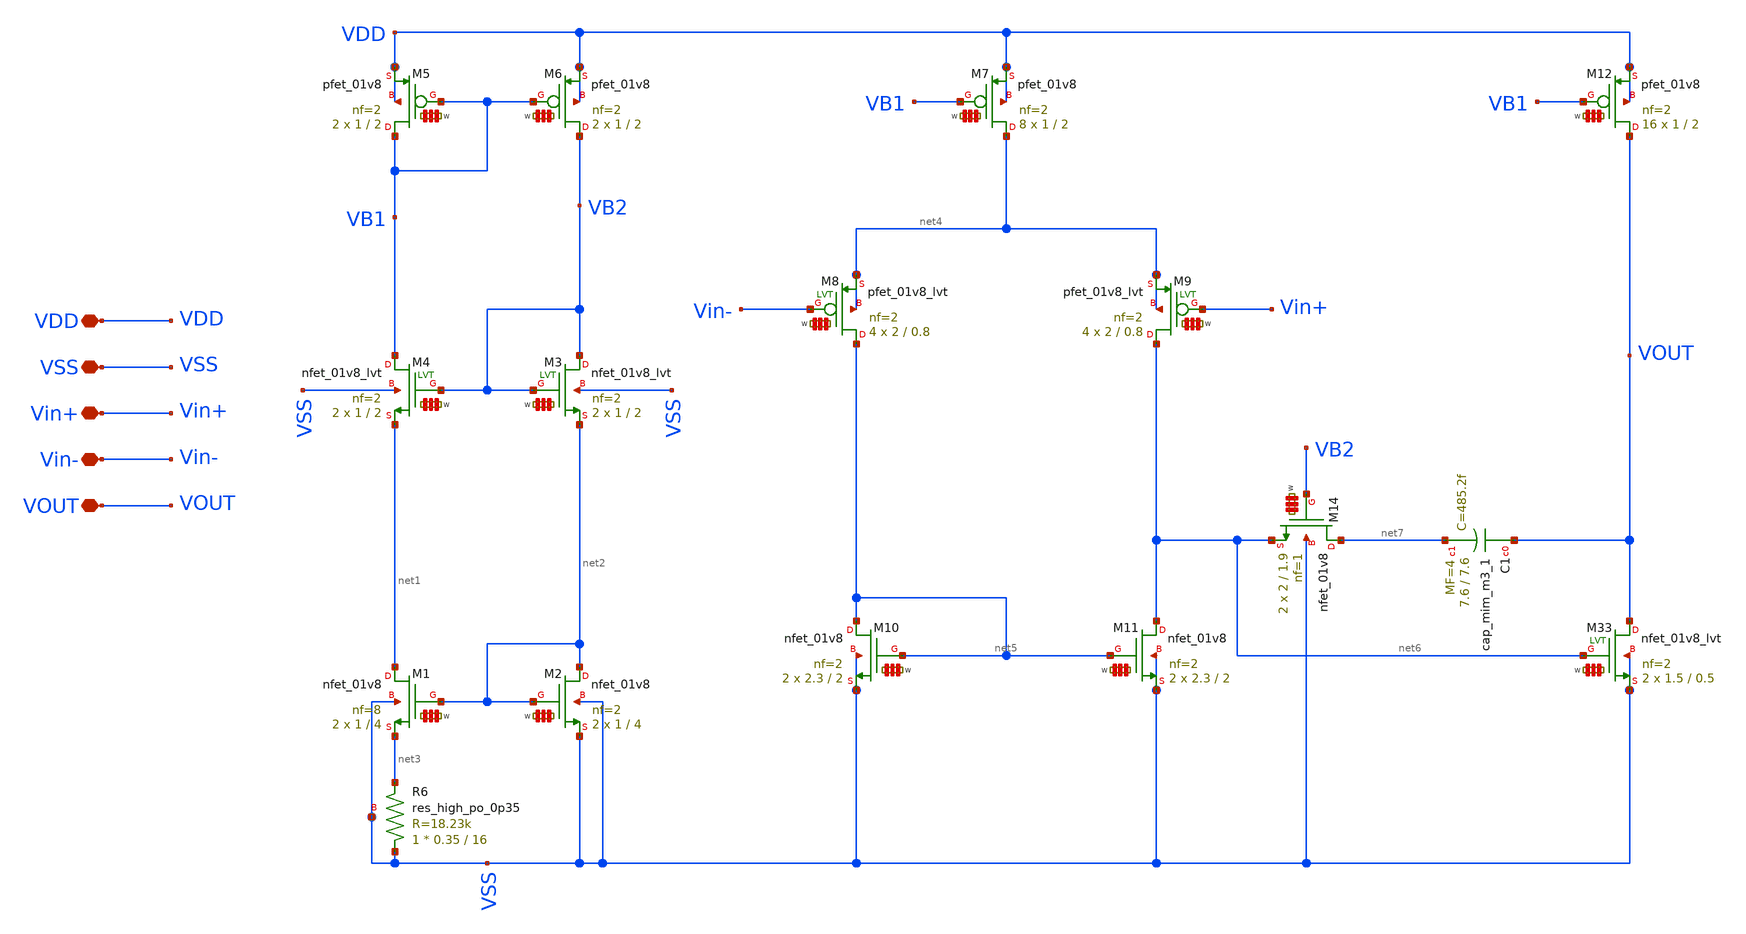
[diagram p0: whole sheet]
** sch_path: LIB/Sky130A/single ended amplifiers/VA001_sky130_1_8V.sch
**.subckt VA001_sky130_1_8V VDD VSS Vin+ Vin- VOUT
*.iopin VDD
*.iopin VSS
*.iopin Vin+
*.iopin Vin-
*.iopin VOUT
XR6 VSS net3 VSS sky130_fd_pr__res_high_po_0p35 L=16 mult=1 m=1
XM1 net1 net2 net3 VSS sky130_fd_pr__nfet_01v8 L=4 W='1 * 8 ' nf=8 ad='int((8 + 1)/2) * 1 / 8 * 0.29'
+ as='int((8 + 2)/2) * 1 / 8 * 0.29' pd='2*int((8 + 1)/2) * (1 / 8 + 0.29)' ps='2*int((8 + 2)/2) * (1 / 8 + 0.29)'
+ nrd='0.29 / 1 ' nrs='0.29 / 1 ' sa=0 sb=0 sd=0 mult=2 m=2
XM2 net2 net2 VSS VSS sky130_fd_pr__nfet_01v8 L=4 W='1 * 2 ' nf=2 ad='int((2 + 1)/2) * 1 / 2 * 0.29'
+ as='int((2 + 2)/2) * 1 / 2 * 0.29' pd='2*int((2 + 1)/2) * (1 / 2 + 0.29)' ps='2*int((2 + 2)/2) * (1 / 2 + 0.29)'
+ nrd='0.29 / 1 ' nrs='0.29 / 1 ' sa=0 sb=0 sd=0 mult=2 m=2
XM5 VB1 VB1 VDD VDD sky130_fd_pr__pfet_01v8 L=2 W='1 * 2 ' nf=2 ad= as='int((2 + 2)/2) * 1 * 0.29' pd='2*int((2 + 1)/2) * (1 + 0.29)'
+ ps='2*int((2 + 2)/2) * (1 + 0.29)' nrd='0.29 / 1 / 2 ' nrs='0.29 / 1 / 2 ' sa=0 sb=0 sd=0 mult=2 m=2
XM6 VB2 VB1 VDD VDD sky130_fd_pr__pfet_01v8 L=2 W='1 * 2 ' nf=2 ad= as='int((2 + 2)/2) * 1 * 0.29' pd='2*int((2 + 1)/2) * (1 + 0.29)'
+ ps='2*int((2 + 2)/2) * (1 + 0.29)' nrd='0.29 / 1 / 2 ' nrs='0.29 / 1 / 2 ' sa=0 sb=0 sd=0 mult=2 m=2
XM7 net4 VB1 VDD VDD sky130_fd_pr__pfet_01v8 L=2 W='1 * 2 ' nf=2 ad= as='int((2 + 2)/2) * 1 * 0.29' pd='2*int((2 + 1)/2) * (1 + 0.29)'
+ ps='2*int((2 + 2)/2) * (1 + 0.29)' nrd='0.29 / 1 / 2 ' nrs='0.29 / 1 / 2 ' sa=0 sb=0 sd=0 mult=8 m=8
XM10 net5 net5 VSS VSS sky130_fd_pr__nfet_01v8 L=2 W='2.3 * 2 ' nf=2 ad='int((2 + 1)/2) * 2.3 / 2 * 0.29'
+ as='int((2 + 2)/2) * 2.3 / 2 * 0.29' pd='2*int((2 + 1)/2) * (2.3 / 2 + 0.29)' ps='2*int((2 + 2)/2) * (2.3 / 2 + 0.29)'
+ nrd='0.29 / 2.3 ' nrs='0.29 / 2.3 ' sa=0 sb=0 sd=0 mult=2 m=2
XM11 net6 net5 VSS VSS sky130_fd_pr__nfet_01v8 L=2 W='2.3 * 2 ' nf=2 ad='int((2 + 1)/2) * 2.3 / 2 * 0.29'
+ as='int((2 + 2)/2) * 2.3 / 2 * 0.29' pd='2*int((2 + 1)/2) * (2.3 / 2 + 0.29)' ps='2*int((2 + 2)/2) * (2.3 / 2 + 0.29)'
+ nrd='0.29 / 2.3 ' nrs='0.29 / 2.3 ' sa=0 sb=0 sd=0 mult=2 m=2
XM12 VOUT VB1 VDD VDD sky130_fd_pr__pfet_01v8 L=2 W='1 * 2 ' nf=2 ad= as='int((2 + 2)/2) * 1 * 0.29'
+ pd='2*int((2 + 1)/2) * (1 + 0.29)' ps='2*int((2 + 2)/2) * (1 + 0.29)' nrd='0.29 / 1 / 2 ' nrs='0.29 / 1 / 2 '
+ sa=0 sb=0 sd=0 mult=16 m=16
XM14 net7 VB2 net6 VSS sky130_fd_pr__nfet_01v8 L=1.9 W='2 * 1 ' nf=1 ad='int((1 + 1)/2) * 2 / 1 * 0.29'
+ as='int((1 + 2)/2) * 2 / 1 * 0.29' pd='2*int((1 + 1)/2) * (2 / 1 + 0.29)' ps='2*int((1 + 2)/2) * (2 / 1 + 0.29)'
+ nrd='0.29 / 2 ' nrs='0.29 / 2 ' sa=0 sb=0 sd=0 mult=2 m=2
XC1 VOUT net7 sky130_fd_pr__cap_mim_m3_1 W=7.6 L=7.6 MF=4 m=4
XM8 net5 Vin- net4 net4 sky130_fd_pr__pfet_01v8_lvt L=0.8 W='2 * 2 ' nf=2 ad='int((2 + 1)/2) * 2 / 2 * 0.29'
+ as='int((2 + 2)/2) * 2 / 2 * 0.29' pd='2*int((2 + 1)/2) * (2 / 2 + 0.29)' ps='2*int((2 + 2)/2) * (2 / 2 + 0.29)'
+ nrd='0.29 / 2 ' nrs='0.29 / 2 ' sa=0 sb=0 sd=0 mult=4 m=4
XM9 net6 Vin+ net4 net4 sky130_fd_pr__pfet_01v8_lvt L=0.8 W='2 * 2 ' nf=2 ad='int((2 + 1)/2) * 2 / 2 * 0.29'
+ as='int((2 + 2)/2) * 2 / 2 * 0.29' pd='2*int((2 + 1)/2) * (2 / 2 + 0.29)' ps='2*int((2 + 2)/2) * (2 / 2 + 0.29)'
+ nrd='0.29 / 2 ' nrs='0.29 / 2 ' sa=0 sb=0 sd=0 mult=4 m=4
XM33 VOUT net6 VSS VSS sky130_fd_pr__nfet_01v8_lvt L=0.5 W='1.5 * 2 ' nf=2 ad='int((2 + 1)/2) * 1.5 / 2 * 0.29'
+ as='int((2 + 2)/2) * 1.5 / 2 * 0.29' pd='2*int((2 + 1)/2) * (1.5 / 2 + 0.29)' ps='2*int((2 + 2)/2) * (1.5 / 2 + 0.29)'
+ nrd='0.29 / 1.5 ' nrs='0.29 / 1.5 ' sa=0 sb=0 sd=0 mult=2 m=2
XM3 VB2 VB2 net2 VSS sky130_fd_pr__nfet_01v8_lvt L=2 W='1 * 2 ' nf=2 ad='int((2 + 1)/2) * 1 / 2 * 0.29'
+ as='int((2 + 2)/2) * 1 / 2 * 0.29' pd='2*int((2 + 1)/2) * (1 / 2 + 0.29)' ps='2*int((2 + 2)/2) * (1 / 2 + 0.29)'
+ nrd='0.29 / 1 ' nrs='0.29 / 1 ' sa=0 sb=0 sd=0 mult=2 m=2
XM4 VB1 VB2 net1 VSS sky130_fd_pr__nfet_01v8_lvt L=2 W='1 * 2 ' nf=2 ad='int((2 + 1)/2) * 1 / 2 * 0.29'
+ as='int((2 + 2)/2) * 1 / 2 * 0.29' pd='2*int((2 + 1)/2) * (1 / 2 + 0.29)' ps='2*int((2 + 2)/2) * (1 / 2 + 0.29)'
+ nrd='0.29 / 1 ' nrs='0.29 / 1 ' sa=0 sb=0 sd=0 mult=2 m=2
**.ends
.end
